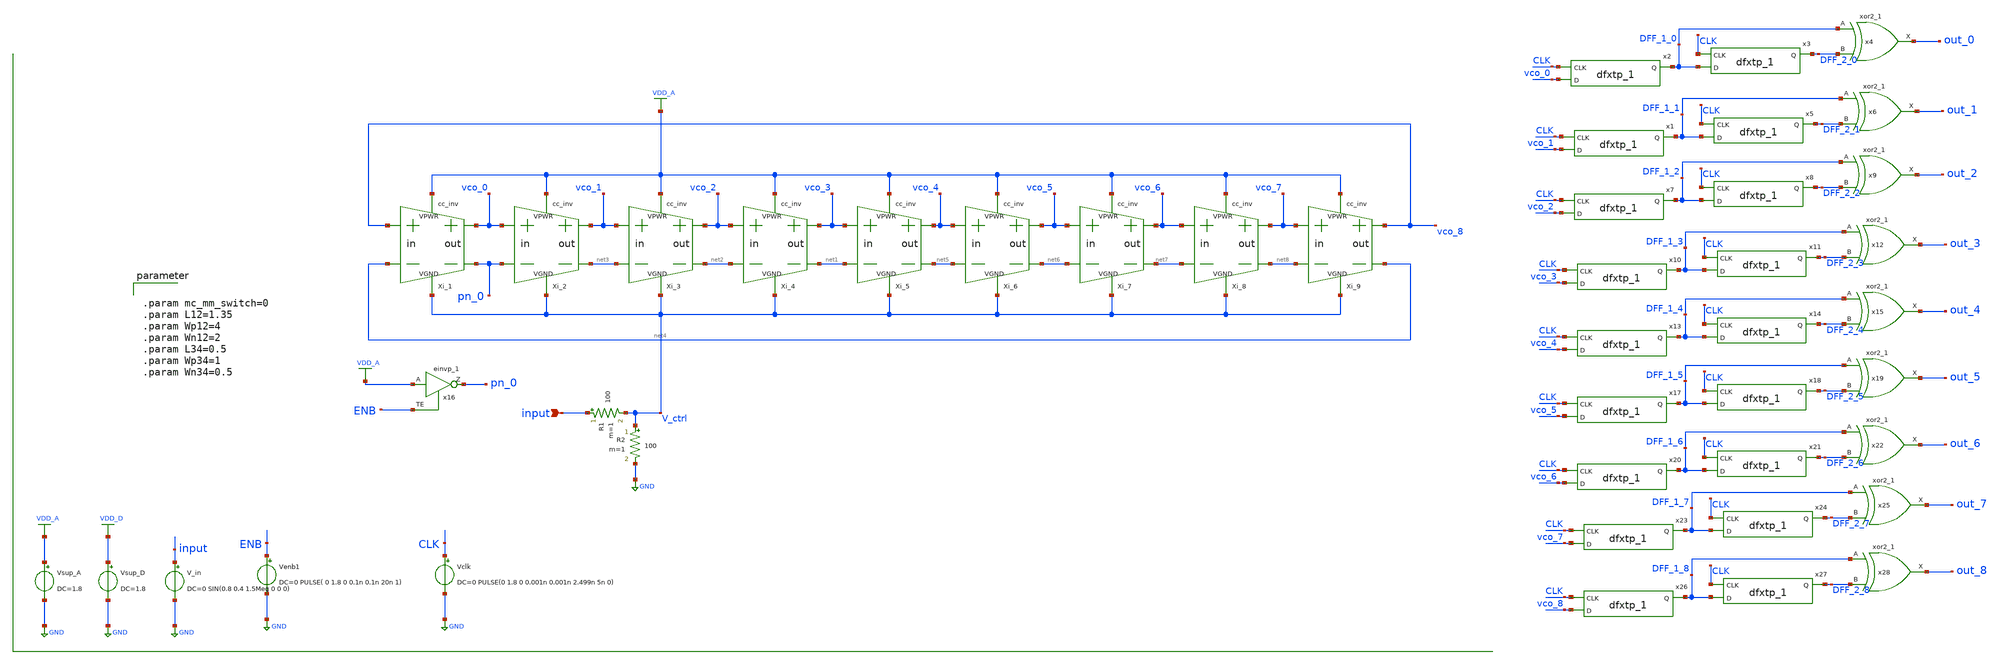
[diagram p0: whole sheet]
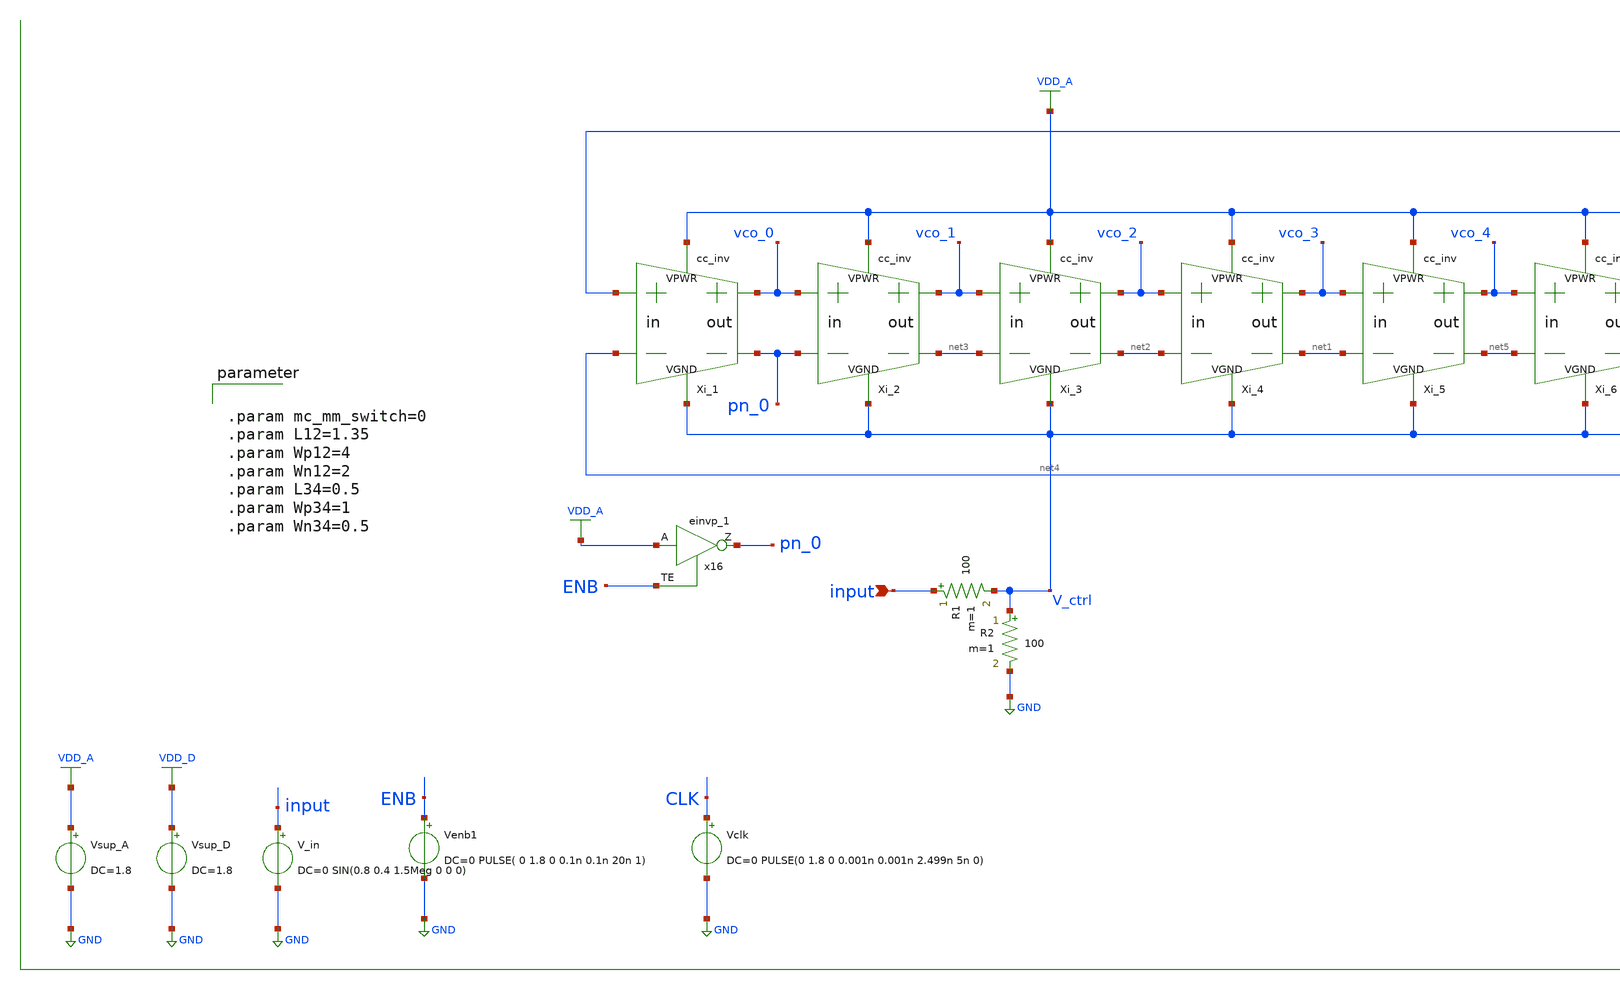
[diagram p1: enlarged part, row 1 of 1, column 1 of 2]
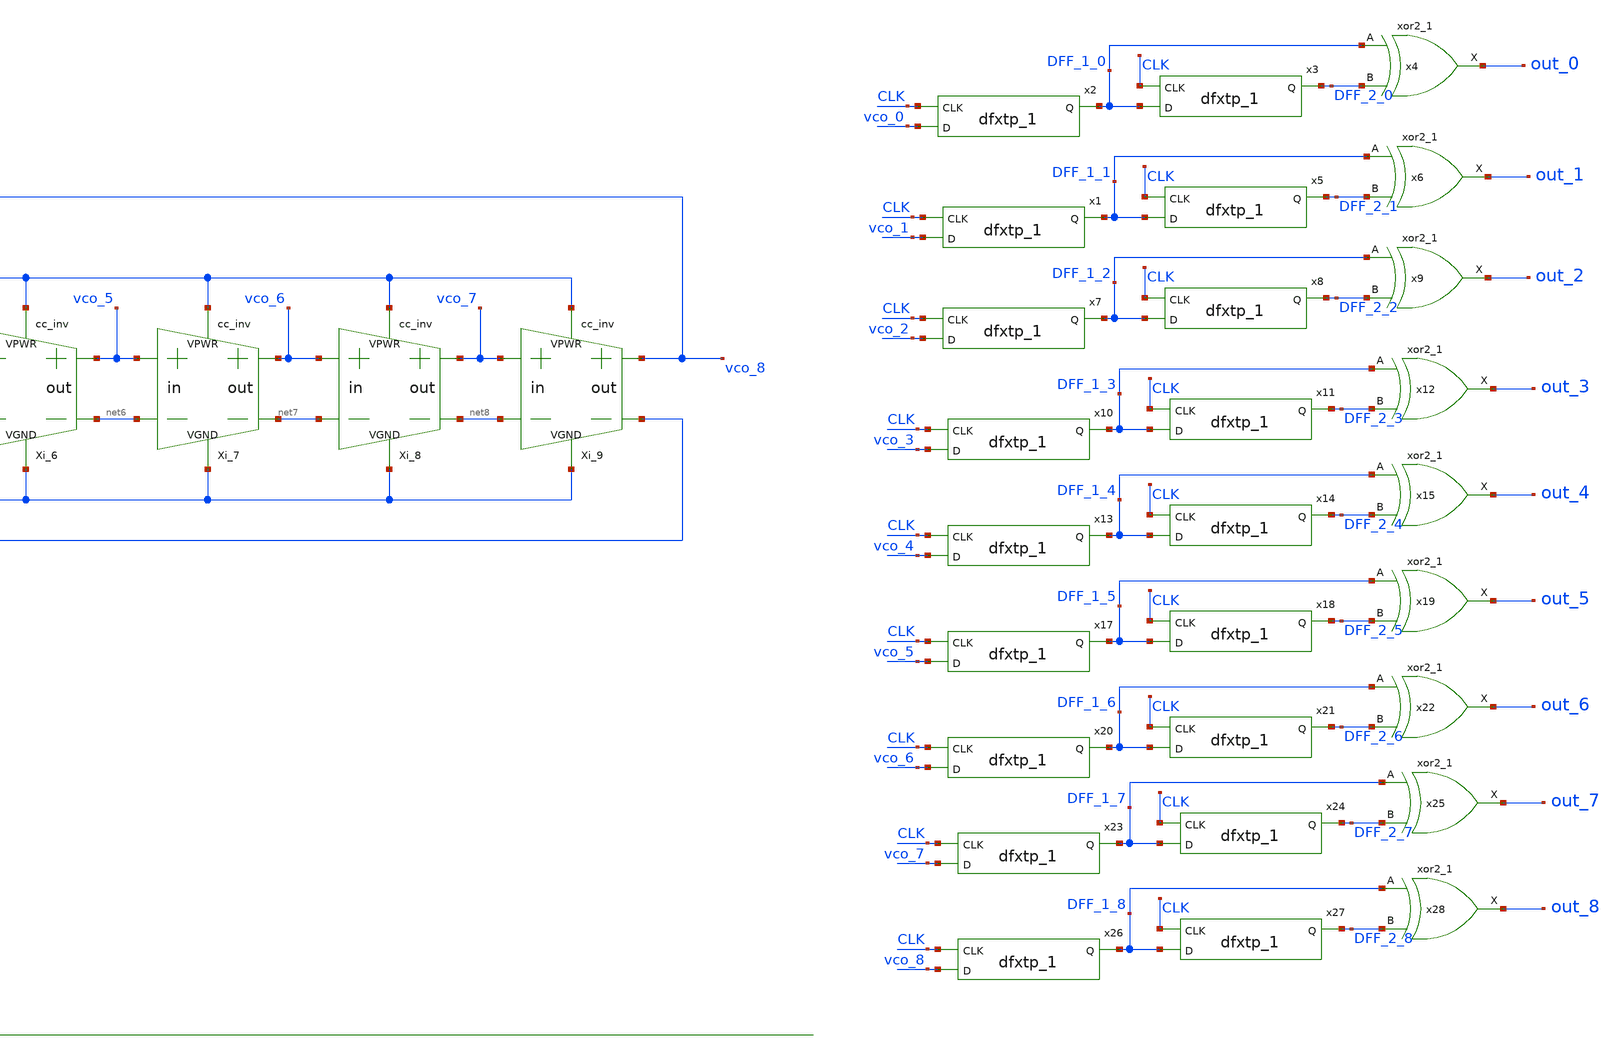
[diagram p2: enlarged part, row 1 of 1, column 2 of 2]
** sch_path: circuit_model/tb/show_all_9.sch
**.subckt show_all_9 input
*.ipin input
Vsup_A VDD_A GND DC=1.8
V_in input GND DC=0 SIN(0.8 0.4 1.5Meg 0 0 0)
Venb1 ENB GND DC=0 PULSE( 0 1.8 0 0.1n 0.1n 20n 1)
R1 input V_ctrl 100 m=1
R2 V_ctrl GND 100 m=1
Vsup_D VDD_D GND DC=1.8
Vclk CLK GND DC=0 PULSE(0 1.8 0 0.001n 0.001n 2.499n 5n 0)
x2 CLK vco_0 GND GND VDD_D VDD_D DFF_1_0 sky130_fd_sc_hd__dfxtp_1
x3 CLK DFF_1_0 GND GND VDD_D VDD_D DFF_2_0 sky130_fd_sc_hd__dfxtp_1
x4 DFF_1_0 DFF_2_0 GND GND VDD_D VDD_D out_0 sky130_fd_sc_hd__xor2_1
x1 CLK vco_1 GND GND VDD_D VDD_D DFF_1_1 sky130_fd_sc_hd__dfxtp_1
x5 CLK DFF_1_1 GND GND VDD_D VDD_D DFF_2_1 sky130_fd_sc_hd__dfxtp_1
x6 DFF_1_1 DFF_2_1 GND GND VDD_D VDD_D out_1 sky130_fd_sc_hd__xor2_1
x7 CLK vco_2 GND GND VDD_D VDD_D DFF_1_2 sky130_fd_sc_hd__dfxtp_1
x8 CLK DFF_1_2 GND GND VDD_D VDD_D DFF_2_2 sky130_fd_sc_hd__dfxtp_1
x9 DFF_1_2 DFF_2_2 GND GND VDD_D VDD_D out_2 sky130_fd_sc_hd__xor2_1
x10 CLK vco_3 GND GND VDD_D VDD_D DFF_1_3 sky130_fd_sc_hd__dfxtp_1
x11 CLK DFF_1_3 GND GND VDD_D VDD_D DFF_2_3 sky130_fd_sc_hd__dfxtp_1
x12 DFF_1_3 DFF_2_3 GND GND VDD_D VDD_D out_3 sky130_fd_sc_hd__xor2_1
x13 CLK vco_4 GND GND VDD_D VDD_D DFF_1_4 sky130_fd_sc_hd__dfxtp_1
x14 CLK DFF_1_4 GND GND VDD_D VDD_D DFF_2_4 sky130_fd_sc_hd__dfxtp_1
x15 DFF_1_4 DFF_2_4 GND GND VDD_D VDD_D out_4 sky130_fd_sc_hd__xor2_1
Xi_1 vco_8 net4 VDD_A V_ctrl vco_0 pn_0 cc_inv L12="L12" Wp12="Wp12" Wn12="Wn12" L34="L34"
+ Wp34="Wp34" Wn34="Wn34"
Xi_2 vco_0 pn_0 VDD_A V_ctrl vco_1 net3 cc_inv L12="L12" Wp12="Wp12" Wn12="Wn12" L34="L34"
+ Wp34="Wp34" Wn34="Wn34"
Xi_3 vco_1 net3 VDD_A V_ctrl vco_2 net2 cc_inv L12="L12" Wp12="Wp12" Wn12="Wn12" L34="L34"
+ Wp34="Wp34" Wn34="Wn34"
Xi_4 vco_2 net2 VDD_A V_ctrl vco_3 net1 cc_inv L12="L12" Wp12="Wp12" Wn12="Wn12" L34="L34"
+ Wp34="Wp34" Wn34="Wn34"
Xi_5 vco_3 net1 VDD_A V_ctrl vco_4 net5 cc_inv L12="L12" Wp12="Wp12" Wn12="Wn12" L34="L34"
+ Wp34="Wp34" Wn34="Wn34"
x16 VDD_A ENB GND GND VDD_A VDD_A pn_0 sky130_fd_sc_hd__einvp_1
Xi_6 vco_4 net5 VDD_A V_ctrl vco_5 net6 cc_inv L12="L12" Wp12="Wp12" Wn12="Wn12" L34="L34"
+ Wp34="Wp34" Wn34="Wn34"
Xi_7 vco_5 net6 VDD_A V_ctrl vco_6 net7 cc_inv L12="L12" Wp12="Wp12" Wn12="Wn12" L34="L34"
+ Wp34="Wp34" Wn34="Wn34"
x17 CLK vco_5 GND GND VDD_D VDD_D DFF_1_5 sky130_fd_sc_hd__dfxtp_1
x18 CLK DFF_1_5 GND GND VDD_D VDD_D DFF_2_5 sky130_fd_sc_hd__dfxtp_1
x19 DFF_1_5 DFF_2_5 GND GND VDD_D VDD_D out_5 sky130_fd_sc_hd__xor2_1
x20 CLK vco_6 GND GND VDD_D VDD_D DFF_1_6 sky130_fd_sc_hd__dfxtp_1
x21 CLK DFF_1_6 GND GND VDD_D VDD_D DFF_2_6 sky130_fd_sc_hd__dfxtp_1
x22 DFF_1_6 DFF_2_6 GND GND VDD_D VDD_D out_6 sky130_fd_sc_hd__xor2_1
Xi_8 vco_6 net7 VDD_A V_ctrl vco_7 net8 cc_inv L12="L12" Wp12="Wp12" Wn12="Wn12" L34="L34"
+ Wp34="Wp34" Wn34="Wn34"
Xi_9 vco_7 net8 VDD_A V_ctrl vco_8 net4 cc_inv L12="L12" Wp12="Wp12" Wn12="Wn12" L34="L34"
+ Wp34="Wp34" Wn34="Wn34"
x23 CLK vco_7 GND GND VDD_D VDD_D DFF_1_7 sky130_fd_sc_hd__dfxtp_1
x24 CLK DFF_1_7 GND GND VDD_D VDD_D DFF_2_7 sky130_fd_sc_hd__dfxtp_1
x25 DFF_1_7 DFF_2_7 GND GND VDD_D VDD_D out_7 sky130_fd_sc_hd__xor2_1
x26 CLK vco_8 GND GND VDD_D VDD_D DFF_1_8 sky130_fd_sc_hd__dfxtp_1
x27 CLK DFF_1_8 GND GND VDD_D VDD_D DFF_2_8 sky130_fd_sc_hd__dfxtp_1
x28 DFF_1_8 DFF_2_8 GND GND VDD_D VDD_D out_8 sky130_fd_sc_hd__xor2_1
**** begin user architecture code


.control
    set nobreak
    set num_threads=10

    save "vdd_a" "vdd_d" @Vsup_a[i] @Vsup_d[i]
    save "input" "V_ctrl"
    save "vco_0" "vco_1" "vco_2" "vco_3" "vco_4" "vco_5" "vco_6" "vco_7" "vco_8"
    save "out_0" "out_1" "out_2" "out_3" "out_4" "out_5" "out_6" "out_7" "out_8"
    save "DFF_1_0" "DFF_2_0"
    save "DFF_1_1" "DFF_2_1"
    save "DFF_1_2" "DFF_2_2"
    save "DFF_1_3" "DFF_2_3"
    save "DFF_1_4" "DFF_2_4"
    save "DFF_1_5" "DFF_2_5"
    save "DFF_1_6" "DFF_2_6"
    save "DFF_1_7" "DFF_2_7"
    save "DFF_1_8" "DFF_2_8"
    save "CLK"
    TRAN 10n 5u

*Calculate Power of system
    MEAS TRAN I_vco AVG @Vsup_a[i] FROM=1u TO=5u
    MEAS TRAN V_vco AVG vdd_a FROM=1u TO=5u
    MEAS TRAN I_qz AVG @Vsup_d[i] FROM=1u TO=5u
    MEAS TRAN V_qz AVG vdd_d FROM=1u TO=5u
    let Power_vco=I_vco*V_vco
    let Power_qz=I_qz*V_qz
    let Power=Power_vco+Power_qz
    echo "The power of system is: "
    print Power

*Calculate Frequency of VCO
    MEAS TRAN prd TRIG vco_0 VAL=0.8 RISE=10 TARG vco_0 VAL=0.8 RISE=20
    let frequency=10/prd
    echo "The AVG frequency of VCO is: "
    print frequency
    plot vco_0+2 CLK+2 DFF_1_0 DFF_2_0 out_0-2

    print vco_0 vco_1 vco_2 > show_all_9/data_vco_0.txt
    print vco_3 vco_4 vco_5 > show_all_9/data_vco_1.txt
    print vco_6 vco_7 vco_8> show_all_9/data_vco_2.txt

    print clk out_0 out_1 > show_all_9/data_out_0.txt
    print out_2 out_3 out_4 > show_all_9/data_out_1.txt
    print out_5 out_6 out_7 > show_all_9/data_out_2.txt
    print out_8 > show_all_9/data_out_3.txt
*    plot input V_ctrl V_ctrl-2 vco_0-2 V_ctrl-4 out_0-4
.endc




** Library on VNU server
.lib /home/dkits/efabless/mpw-5/pdks/sky130A/libs.tech/ngspice/sky130.lib.spice tt
.inc /home/dkits/efabless/mpw-5/pdks/sky130A/libs.ref/sky130_fd_sc_hd/spice/sky130_fd_sc_hd.spice




.param mc_mm_switch=0
.param L12=1.35
.param Wp12=4
.param Wn12=2
.param L34=0.5
.param Wp34=1
.param Wn34=0.5


**** end user architecture code
**.ends

* expanding   symbol:  /home/userdata/k63D/toind_63d/Desktop/project/circuit_model/lib/cc_inv.sym #
*+ of pins=6
** sym_path: circuit_model/lib/cc_inv.sym
** sch_path: circuit_model/lib/cc_inv.sch
.subckt cc_inv inp inn VPWR VGND outp outn  L12=0.15 Wp12=1.2 Wn12=0.65 L34=0.15 Wp34=1.2 Wn34=0.65
*.opin outp
*.ipin inn
*.iopin VGND
*.opin outn
*.ipin inp
*.iopin VPWR
Xi_1 inp VPWR VGND outp inverter L="L12" Wp="Wp12" Np=1 Wn="Wn12" Nn=1
Xi_3 outp VPWR VGND outn inverter L="L34" Wp="Wp34" Np=1 Wn="Wn34" Nn=1
Xi_2 inn VPWR VGND outn inverter L="L12" Wp="Wp12" Np=1 Wn="Wn12" Nn=1
Xi_4 outn VPWR VGND outp inverter L="L34" Wp="Wp34" Np=1 Wn="Wn34" Nn=1
.ends


* expanding   symbol:  inverter.sym # of pins=4
** sym_path: circuit_model/lib/inverter.sym
** sch_path: circuit_model/lib/inverter.sch
.subckt inverter A VPWR VGND Y  L=0.15 Wp=1.2 Np=1 Wn=0.65 Nn=1
*.iopin VPWR
*.iopin VGND
*.ipin A
*.opin Y
XM1 Y A VPWR VDD sky130_fd_pr__pfet_01v8 L="L" W="Wp" nf="Np" ad='int(("Np" + 1)/2) * "Wp" / "Np" * 0.29'
+ as='int(("Np" + 2)/2) * "Wp" / "Np" * 0.29' pd='2*int(("Np" + 1)/2) * ("Wp" / "Np" + 0.29)' ps='2*int(("Np" + 2)/2) * ("Wp" / "Np" + 0.29)'
+ nrd='0.29 / "Wp" ' nrs='0.29 / "Wp" ' sa=0 sb=0 sd=0 mult=1 m=1
XM2 Y A VGND GND sky130_fd_pr__nfet_01v8 L="L" W="Wn" nf="Nn" ad='int((nf+1)/2) * W/nf * 0.29' as='int((nf+2)/2) * W/nf * 0.29'
+ pd='2*int((nf+1)/2) * (W/nf + 0.29)' ps='2*int((nf+2)/2) * (W/nf + 0.29)' nrd='0.29 / W' nrs='0.29 / W'
+ sa=0 sb=0 sd=0 mult=1 m=1
.ends

.GLOBAL VDD_A
.GLOBAL GND
.GLOBAL VDD_D
.end
